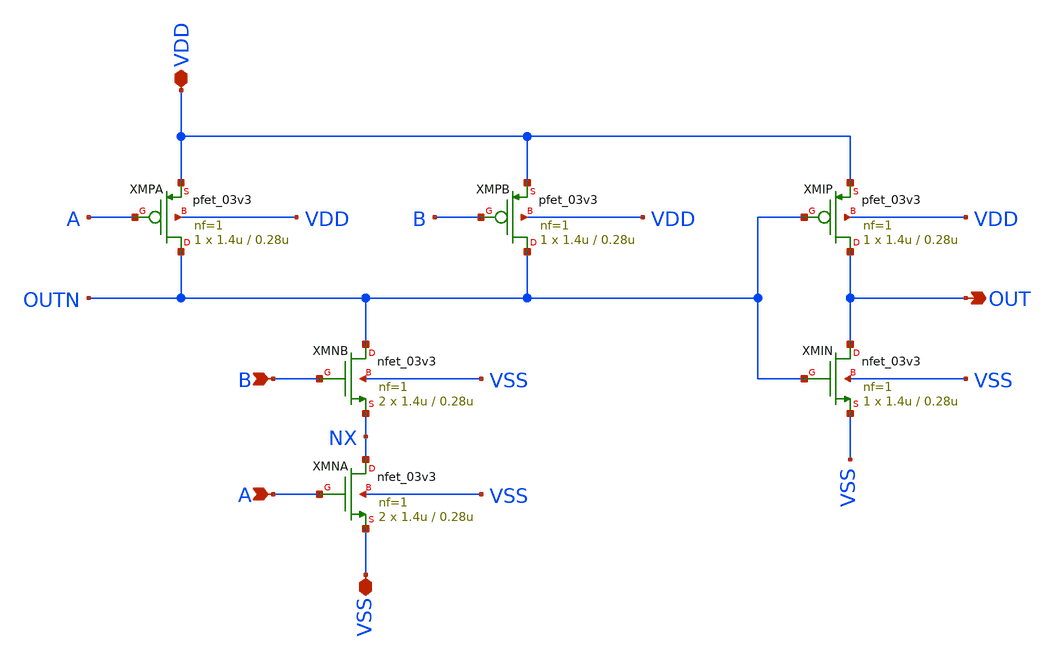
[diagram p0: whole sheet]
** sch_path: designs/gate_and/xschem/gate_and.sch
**.subckt gate_and OUT A VDD VSS B
*.opin OUT
*.ipin A
*.iopin VDD
*.iopin VSS
*.ipin B
XMNB OUTN B NX VSS nfet_03v3 L=0.28u W=1.4u nf=1 ad='int((nf+1)/2) * W/nf * 0.18u' as='int((nf+2)/2) * W/nf * 0.18u'
+ pd='2*int((nf+1)/2) * (W/nf + 0.18u)' ps='2*int((nf+2)/2) * (W/nf + 0.18u)' nrd='0.18u / W' nrs='0.18u / W'
+ sa=0 sb=0 sd=0 m=2
XMPB OUTN B VDD VDD pfet_03v3 L=0.28u W=1.4u nf=1 ad='int((nf+1)/2) * W/nf * 0.18u' as='int((nf+2)/2) * W/nf * 0.18u'
+ pd='2*int((nf+1)/2) * (W/nf + 0.18u)' ps='2*int((nf+2)/2) * (W/nf + 0.18u)' nrd='0.18u / W' nrs='0.18u / W'
+ sa=0 sb=0 sd=0 m=1
XMNA NX A VSS VSS nfet_03v3 L=0.28u W=1.4u nf=1 ad='int((nf+1)/2) * W/nf * 0.18u' as='int((nf+2)/2) * W/nf * 0.18u'
+ pd='2*int((nf+1)/2) * (W/nf + 0.18u)' ps='2*int((nf+2)/2) * (W/nf + 0.18u)' nrd='0.18u / W' nrs='0.18u / W'
+ sa=0 sb=0 sd=0 m=2
XMPA OUTN A VDD VDD pfet_03v3 L=0.28u W=1.4u nf=1 ad='int((nf+1)/2) * W/nf * 0.18u' as='int((nf+2)/2) * W/nf * 0.18u'
+ pd='2*int((nf+1)/2) * (W/nf + 0.18u)' ps='2*int((nf+2)/2) * (W/nf + 0.18u)' nrd='0.18u / W' nrs='0.18u / W'
+ sa=0 sb=0 sd=0 m=1
XMIN OUT OUTN VSS VSS nfet_03v3 L=0.28u W=1.4u nf=1 ad='int((nf+1)/2) * W/nf * 0.18u' as='int((nf+2)/2) * W/nf * 0.18u'
+ pd='2*int((nf+1)/2) * (W/nf + 0.18u)' ps='2*int((nf+2)/2) * (W/nf + 0.18u)' nrd='0.18u / W' nrs='0.18u / W'
+ sa=0 sb=0 sd=0 m=1
XMIP OUT OUTN VDD VDD pfet_03v3 L=0.28u W=1.4u nf=1 ad='int((nf+1)/2) * W/nf * 0.18u' as='int((nf+2)/2) * W/nf * 0.18u'
+ pd='2*int((nf+1)/2) * (W/nf + 0.18u)' ps='2*int((nf+2)/2) * (W/nf + 0.18u)' nrd='0.18u / W' nrs='0.18u / W'
+ sa=0 sb=0 sd=0 m=1
**.ends
.end
